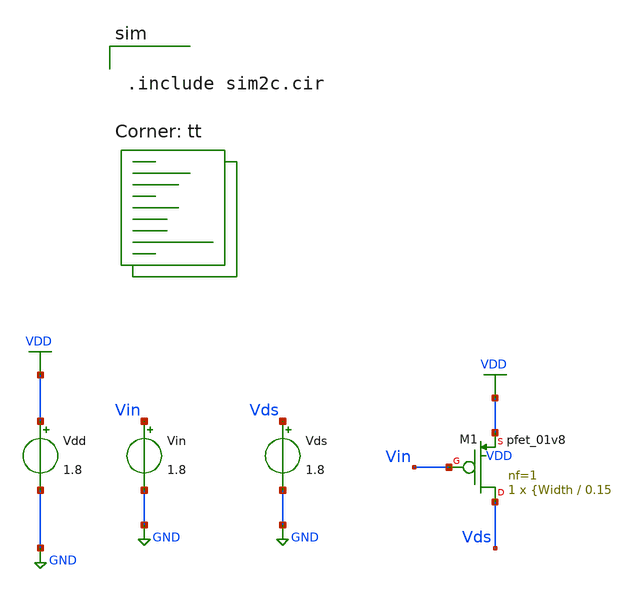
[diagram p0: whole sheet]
** sch_path: assignments/assignment1/assign2c.sch
**.subckt assign2c
Vdd VDD GND 1.8
XM1 Vds Vin VDD VDD sky130_fd_pr__pfet_01v8 L=0.15 W={Width nf=1 ad='int((1 + 1)/2) * {Width / 1 * 0.29'
+ as='int((1 + 2)/2) * {Width / 1 * 0.29' pd='2*int((1 + 1)/2) * ({Width / 1 + 0.29)' ps='2*int((1 + 2)/2) * ({Width
+ / 1 + 0.29)' nrd='0.29 / {Width ' nrs='0.29 / {Width ' sa=0 sb=0 sd=0 mult=1 m=1
Vin Vin GND 1.8
Vds Vds GND 1.8
**** begin user architecture code


.include sim2c.cir


.lib $::SKYWATER_MODELS/sky130.lib.spice tt
**** end user architecture code
**.ends
.GLOBAL GND
.GLOBAL VDD
.end
